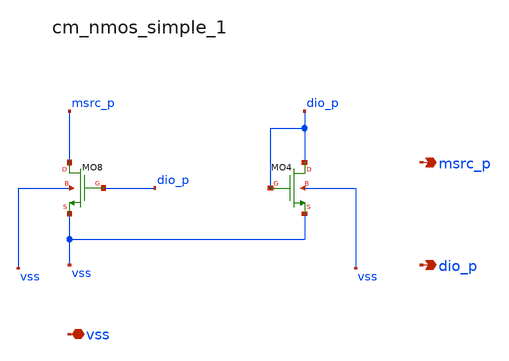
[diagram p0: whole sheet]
** sch_path: analog-db/raw/ia_001_hsu_bandpass_classab/hier/blocks/cm_nmos_simple_1.sch
**.subckt cm_nmos_simple_1 vss msrc_p dio_p
*.iopin vss
*.opin msrc_p
*.opin dio_p
XMO4 dio_p dio_p vss vss sg13_lv_nmos w=x_dut_xmo4_w l=x_dut_xmo4_l ng=1 m=x_dut_xmo4_m
XMO8 msrc_p dio_p vss vss sg13_lv_nmos w=x_dut_xmo8_w l=x_dut_xmo8_l ng=1 m=x_dut_xmo8_m
**.ends
.end
